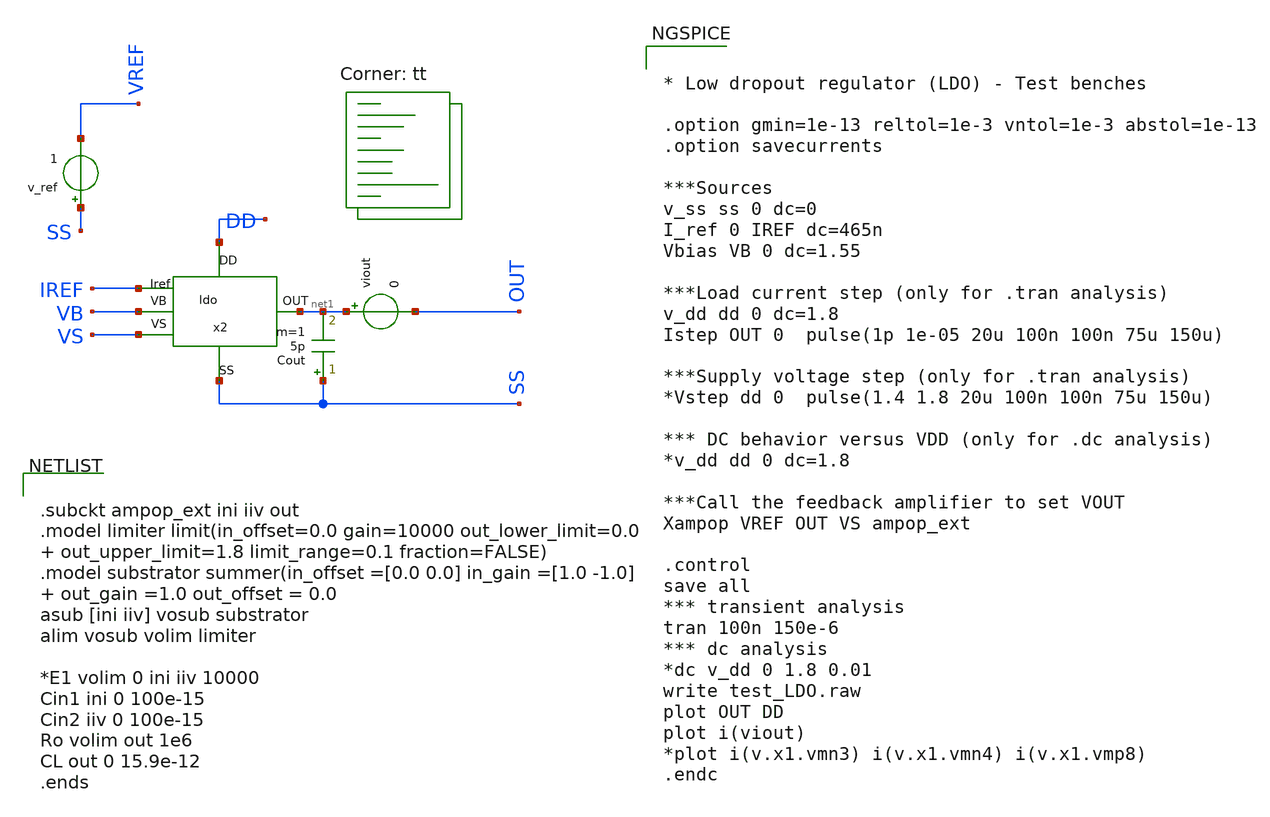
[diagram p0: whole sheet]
** sch_path: xschem/test_ldo.sch
**.subckt test_ldo
Cout SS net1 5p m=1
viout net1 OUT 0
v_ref SS VREF 1
x2 net1 DD SS VB VS IREF ldo
**** begin user architecture code
.lib $::SKYWATER_MODELS/sky130.lib.spice tt


* Low dropout regulator (LDO) - Test benches

.option gmin=1e-13 reltol=1e-3 vntol=1e-3 abstol=1e-13
.option savecurrents

***Sources
v_ss ss 0 dc=0
I_ref 0 IREF dc=465n
Vbias VB 0 dc=1.55

***Load current step (only for .tran analysis)
v_dd dd 0 dc=1.8
Istep OUT 0  pulse(1p 1e-05 20u 100n 100n 75u 150u)

***Supply voltage step (only for .tran analysis)
*Vstep dd 0  pulse(1.4 1.8 20u 100n 100n 75u 150u)

*** DC behavior versus VDD (only for .dc analysis)
*v_dd dd 0 dc=1.8

***Call the feedback amplifier to set VOUT
Xampop VREF OUT VS ampop_ext

.control
save all
*** transient analysis
tran 100n 150e-6
*** dc analysis
*dc v_dd 0 1.8 0.01
write test_LDO.raw
plot OUT DD
plot i(viout)
*plot i(v.x1.vmn3) i(v.x1.vmn4) i(v.x1.vmp8)
.endc




.subckt ampop_ext ini iiv out
.model limiter limit(in_offset=0.0 gain=10000 out_lower_limit=0.0  out_upper_limit=1.8
+ limit_range=0.1 fraction=FALSE)
.model substrator summer(in_offset =[0.0 0.0] in_gain =[1.0 -1.0]  out_gain =1.0 out_offset = 0.0
asub [ini iiv] vosub substrator
alim vosub volim limiter

*E1 volim 0 ini iiv 10000
Cin1 ini 0 100e-15
Cin2 iiv 0 100e-15
Ro volim out 1e6
CL out 0 15.9e-12
.ends


**** end user architecture code
**.ends

* expanding   symbol:  ldo.sym # of pins=6
** sym_path: xschem/ldo.sym
** sch_path: xschem/ldo.sch
.subckt ldo OUT DD SS VB VS Iref
*.iopin DD
*.ipin Iref
*.opin OUT
*.ipin VB
*.ipin VS
*.iopin SS
XMN1 net3 VB net1 SS sky130_fd_pr__nfet_01v8_lvt L=1.43 W=5.19 nf=1 ad='int((nf+1)/2) * W/nf * 0.29'
+ as='int((nf+2)/2) * W/nf * 0.29' pd='2*int((nf+1)/2) * (W/nf + 0.29)' ps='2*int((nf+2)/2) * (W/nf + 0.29)'
+ nrd='0.29 / W' nrs='0.29 / W' sa=0 sb=0 sd=0 mult=2 m=2
XMN2c net1 Iref SS SS sky130_fd_pr__nfet_01v8_lvt L=0.66 W=5.10 nf=1 ad='int((nf+1)/2) * W/nf * 0.29'
+ as='int((nf+2)/2) * W/nf * 0.29' pd='2*int((nf+1)/2) * (W/nf + 0.29)' ps='2*int((nf+2)/2) * (W/nf + 0.29)'
+ nrd='0.29 / W' nrs='0.29 / W' sa=0 sb=0 sd=0 mult=4 m=4
XMN2b net2 Iref SS SS sky130_fd_pr__nfet_01v8_lvt L=0.66 W=5.10 nf=1 ad='int((nf+1)/2) * W/nf * 0.29'
+ as='int((nf+2)/2) * W/nf * 0.29' pd='2*int((nf+1)/2) * (W/nf + 0.29)' ps='2*int((nf+2)/2) * (W/nf + 0.29)'
+ nrd='0.29 / W' nrs='0.29 / W' sa=0 sb=0 sd=0 mult=2 m=2
XMN2a Iref Iref SS SS sky130_fd_pr__nfet_01v8_lvt L=0.66 W=5.10 nf=1 ad='int((nf+1)/2) * W/nf * 0.29'
+ as='int((nf+2)/2) * W/nf * 0.29' pd='2*int((nf+1)/2) * (W/nf + 0.29)' ps='2*int((nf+2)/2) * (W/nf + 0.29)'
+ nrd='0.29 / W' nrs='0.29 / W' sa=0 sb=0 sd=0 mult=2 m=2
XMP2 net1 VS OUT OUT sky130_fd_pr__pfet_01v8_lvt L=1.27 W=6.07 nf=1 ad='int((nf+1)/2) * W/nf * 0.29'
+ as='int((nf+2)/2) * W/nf * 0.29' pd='2*int((nf+1)/2) * (W/nf + 0.29)' ps='2*int((nf+2)/2) * (W/nf + 0.29)'
+ nrd='0.29 / W' nrs='0.29 / W' sa=0 sb=0 sd=0 mult=2 m=2
XMP1 OUT net3 DD DD sky130_fd_pr__pfet_01v8_lvt L=0.37 W=5.17 nf=1 ad='int((1 + 1)/2) * 5.17 / 1 * 0.29'
+ as='int((1 + 2)/2) * 5.17 / 1 * 0.29' pd='2*int((1 + 1)/2) * (5.17 / 1 + 0.29)' ps='2*int((1 + 2)/2) * (5.17 / 1 + 0.29)'
+ nrd='0.29 / 5.17 ' nrs='0.29 / 5.17 ' sa=0 sb=0 sd=0 mult=1 m=1
XMP3b net3 net2 DD DD sky130_fd_pr__pfet_01v8 L=3.89 W=0.89 nf=1 ad='int((nf+1)/2) * W/nf * 0.29' as='int((nf+2)/2) * W/nf * 0.29'
+ pd='2*int((nf+1)/2) * (W/nf + 0.29)' ps='2*int((nf+2)/2) * (W/nf + 0.29)' nrd='0.29 / W' nrs='0.29 / W'
+ sa=0 sb=0 sd=0 mult=2 m=2
XMP3a net2 net2 DD DD sky130_fd_pr__pfet_01v8 L=3.89 W=0.89 nf=1 ad='int((nf+1)/2) * W/nf * 0.29' as='int((nf+2)/2) * W/nf * 0.29'
+ pd='2*int((nf+1)/2) * (W/nf + 0.29)' ps='2*int((nf+2)/2) * (W/nf + 0.29)' nrd='0.29 / W' nrs='0.29 / W'
+ sa=0 sb=0 sd=0 mult=2 m=2
XC1 net3 OUT sky130_fd_pr__cap_mim_m3_1 W=4 L=15 MF=1 m=1
XMP3 DD DD DD DD sky130_fd_pr__pfet_01v8 L=3.89 W=0.89 nf=1 ad='int((nf+1)/2) * W/nf * 0.29' as='int((nf+2)/2) * W/nf * 0.29'
+ pd='2*int((nf+1)/2) * (W/nf + 0.29)' ps='2*int((nf+2)/2) * (W/nf + 0.29)' nrd='0.29 / W' nrs='0.29 / W'
+ sa=0 sb=0 sd=0 mult=2 m=2
XMN2 SS SS SS SS sky130_fd_pr__nfet_01v8_lvt L=0.66 W=5.10 nf=1 ad='int((nf+1)/2) * W/nf * 0.29' as='int((nf+2)/2) * W/nf * 0.29'
+ pd='2*int((nf+1)/2) * (W/nf + 0.29)' ps='2*int((nf+2)/2) * (W/nf + 0.29)' nrd='0.29 / W' nrs='0.29 / W'
+ sa=0 sb=0 sd=0 mult=2 m=2
.ends

.end
